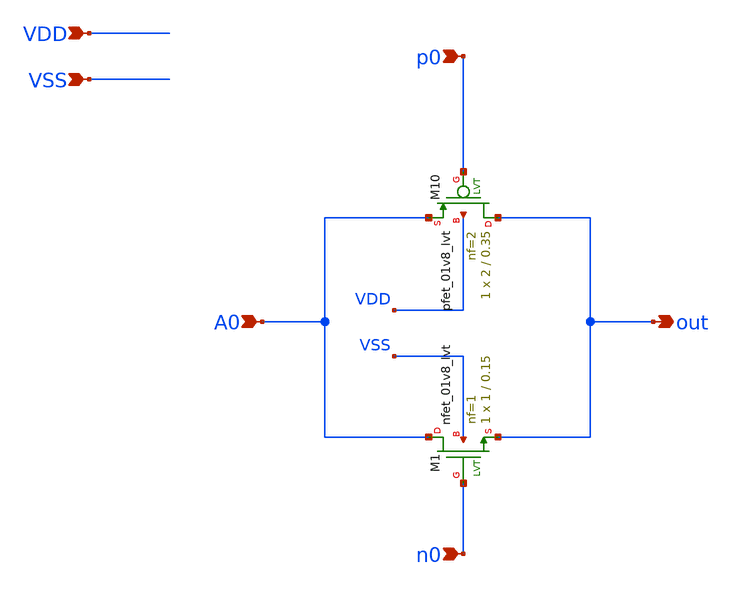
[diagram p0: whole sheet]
** sch_path: xschem/Utili/Passgate_debug.sch
**.subckt Passgate_debug VDD VSS p0 n0 A0 out
*.ipin VDD
*.ipin VSS
*.ipin p0
*.ipin n0
*.ipin A0
*.opin out
XM10 out p0 A0 VDD sky130_fd_pr__pfet_01v8_lvt L=0.35 W=2 nf=2 ad='int((2 + 1)/2) * 2 / 2 * 0.29' as='int((2 + 2)/2) * 2 / 2 * 0.29'
+ pd='2*int((2 + 1)/2) * (2 / 2 + 0.29)' ps='2*int((2 + 2)/2) * (2 / 2 + 0.29)' nrd='0.29 / 2 ' nrs='0.29 / 2 '
+ sa=0 sb=0 sd=0 mult=1 m=1
XM1 A0 n0 out VSS sky130_fd_pr__nfet_01v8_lvt L=0.15 W=1 nf=1 ad='int((1 + 1)/2) * 1 / 1 * 0.29' as='int((1 + 2)/2) * 1 / 1 * 0.29'
+ pd='2*int((1 + 1)/2) * (1 / 1 + 0.29)' ps='2*int((1 + 2)/2) * (1 / 1 + 0.29)' nrd='0.29 / 1 ' nrs='0.29 / 1 '
+ sa=0 sb=0 sd=0 mult=1 m=1
**.ends
.end
